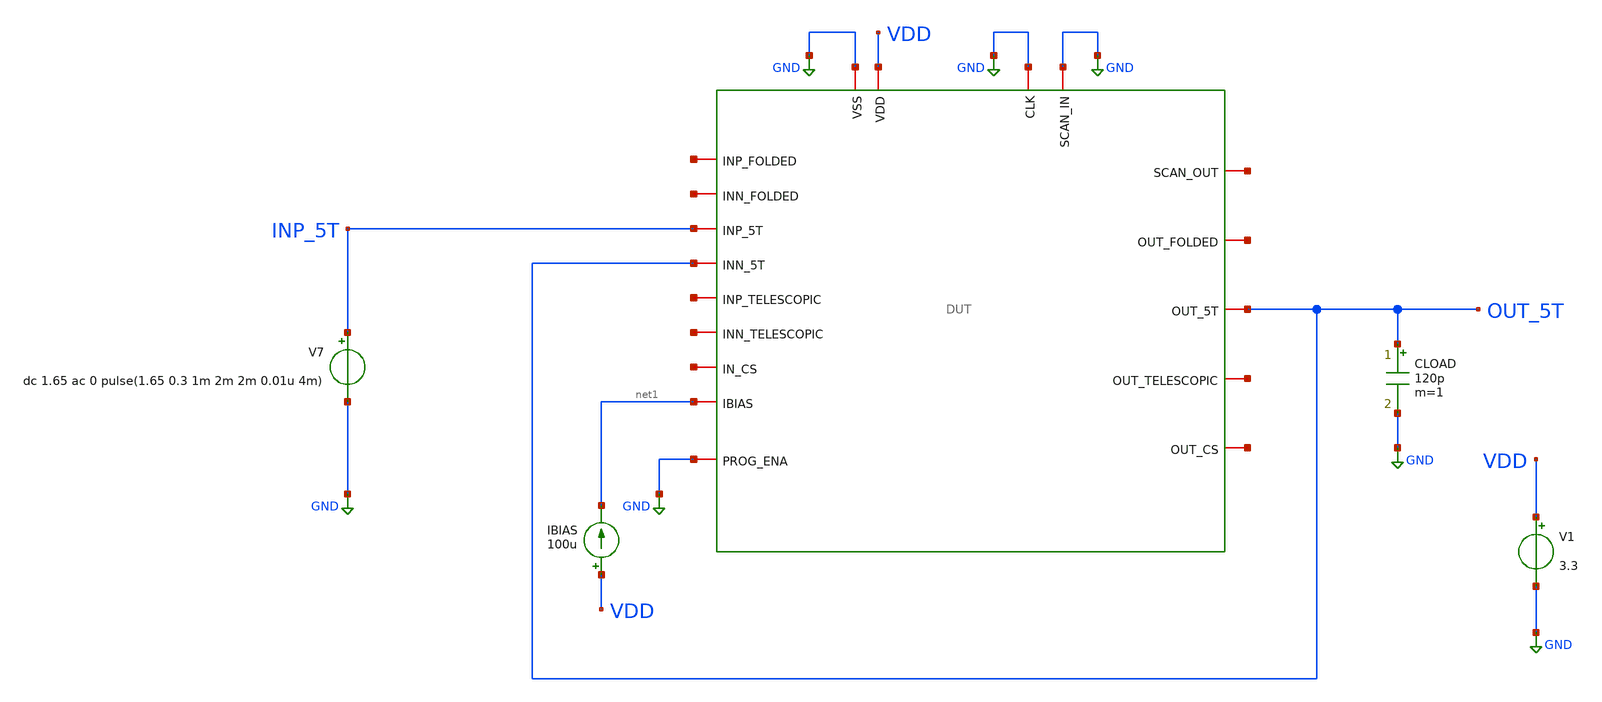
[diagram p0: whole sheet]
** sch_path: designs/libs/verification/ota_5t/defult_sizing/5t_large_signal_lower_swing_tb.sch
**.subckt 5t_large_signal_lower_swing_tb
x1 GND net2 GND GND VDD net3 net4 OUT_5T net1 net5 INP_5T OUT_5T net6 net7 net8 net9 net10 GND DUT
V1 VDD GND 3.3
CLOAD OUT_5T GND 120p m=1
V7 INP_5T GND dc 1.65 ac 0 pulse(1.65 0.3 1m 2m 2m 0.01u 4m)
IBIAS VDD net1 100u
**** begin user architecture code

.include $::180MCU_MODELS/design.ngspice
.lib $::180MCU_MODELS/sm141064.ngspice typical



.control
tran 1u 5m

set color0 = white
set color1 = black
plot v(out_5T) v(inp_5T)

let error = v(out_5T) - v(inp_5T)
plot error

meas tran t_clip when error = 0.019 cross = 1
print t_clip

meas tran vout_clip find v(out_5T) at = t_clip
meas tran vin_clip find v(inp_5T) at = t_clip
print vout_clip vin_clip
.endc


**** end user architecture code
**.ends
.GLOBAL GND
.end
